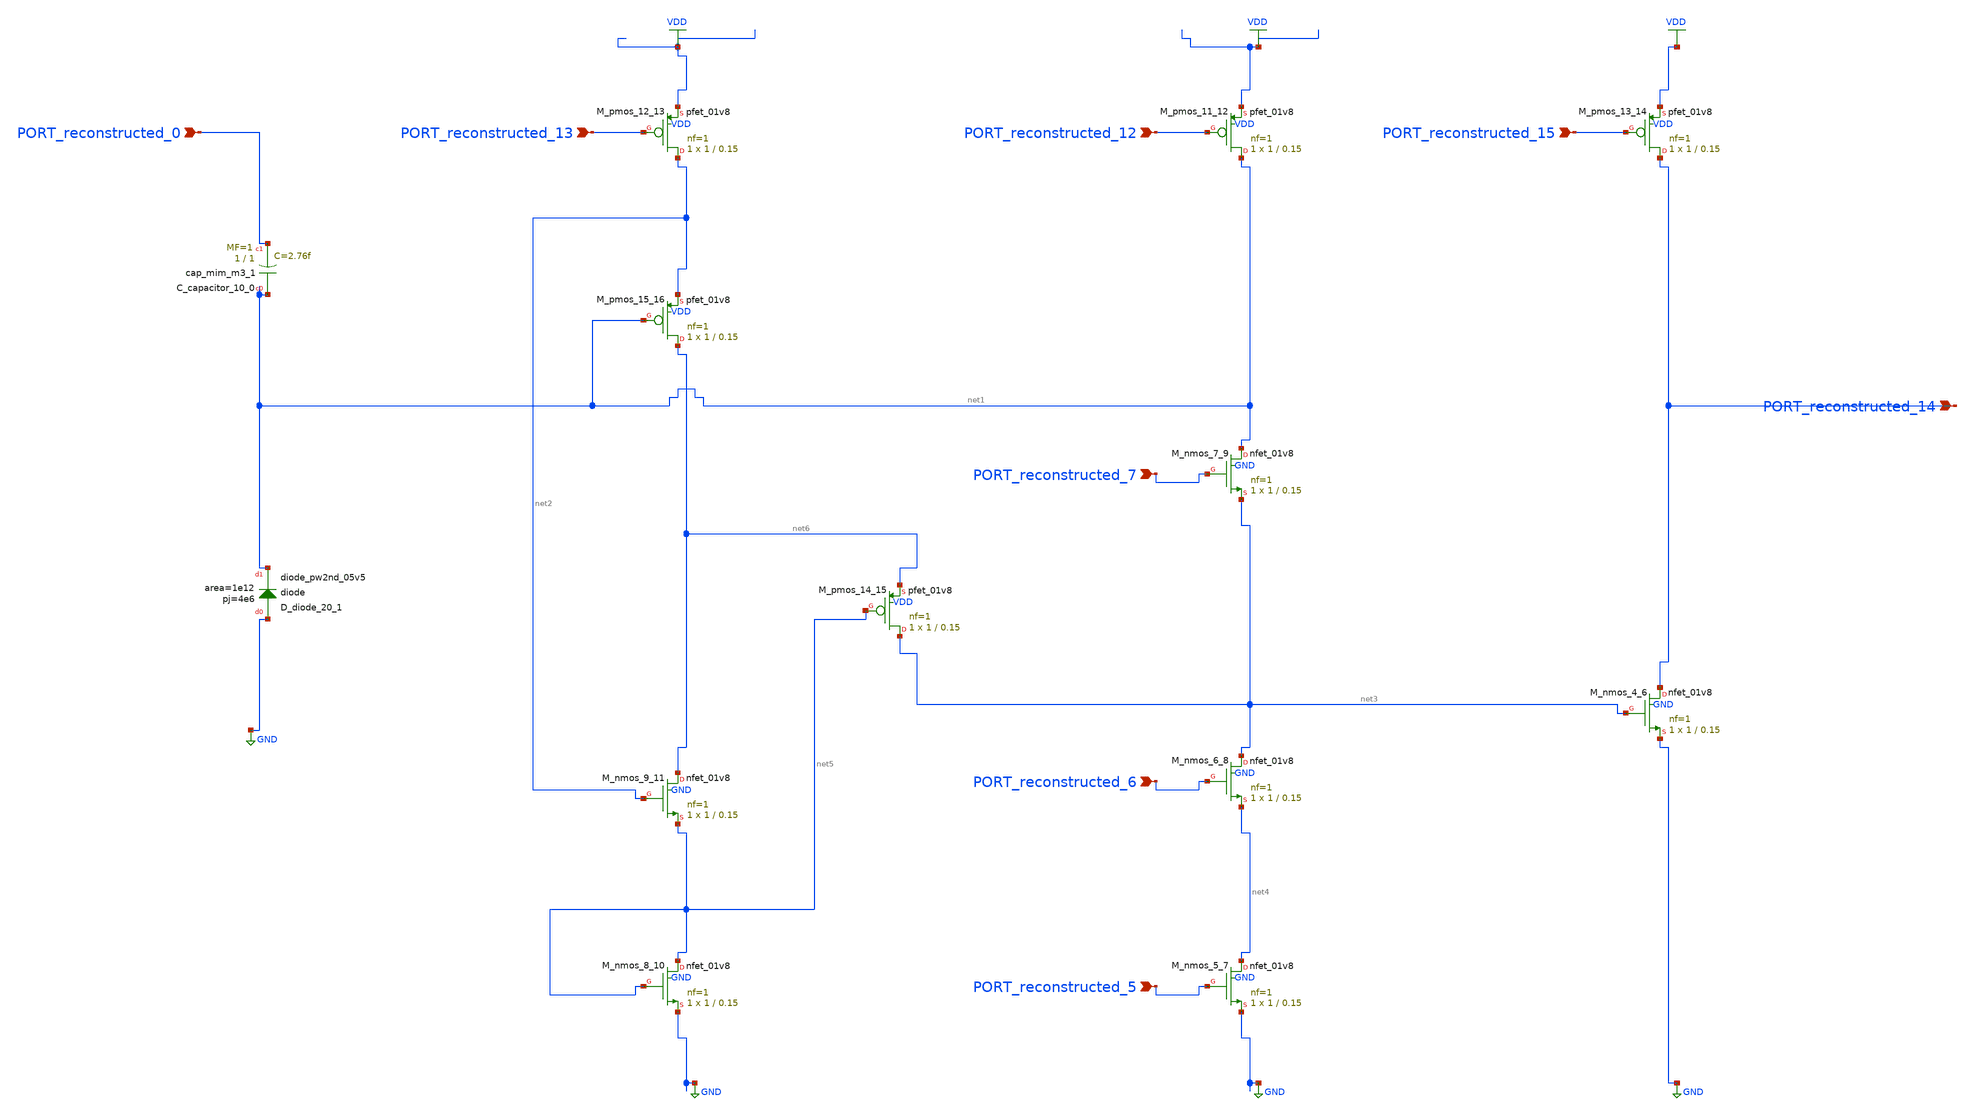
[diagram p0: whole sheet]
** sch_path: schematics/SchemGen/10_22323_1_420_0083_05_001.sch
**.subckt 10_22323_1_420_0083_05_001 PORT_reconstructed_6 PORT_reconstructed_12 PORT_reconstructed_7
*+ PORT_reconstructed_15 PORT_reconstructed_5 PORT_reconstructed_13 PORT_reconstructed_0 PORT_reconstructed_14
*.ipin PORT_reconstructed_6
*.ipin PORT_reconstructed_12
*.ipin PORT_reconstructed_7
*.ipin PORT_reconstructed_15
*.ipin PORT_reconstructed_5
*.ipin PORT_reconstructed_13
*.ipin PORT_reconstructed_0
*.ipin PORT_reconstructed_14
XC_capacitor_10_0 net1 PORT_reconstructed_0 sky130_fd_pr__cap_mim_m3_1 W=1 L=1 MF=1 m=1
XD_diode_20_1 GND net1 sky130_fd_pr__diode_pw2nd_05v5 area=1e12 pj=4e6
XM_nmos_4_6 PORT_reconstructed_14 net3 GND GND sky130_fd_pr__nfet_01v8 L=0.15 W=1 nf=1 ad='int((1 + 1)/2) * 1 / 1 * 0.29'
+ as='int((1 + 2)/2) * 1 / 1 * 0.29' pd='2*int((1 + 1)/2) * (1 / 1 + 0.29)' ps='2*int((1 + 2)/2) * (1 / 1 + 0.29)'
+ nrd='0.29 / 1 ' nrs='0.29 / 1 ' sa=0 sb=0 sd=0 mult=1 m=1
XM_nmos_5_7 net4 PORT_reconstructed_5 GND GND sky130_fd_pr__nfet_01v8 L=0.15 W=1 nf=1 ad='int((1 + 1)/2) * 1 / 1 * 0.29'
+ as='int((1 + 2)/2) * 1 / 1 * 0.29' pd='2*int((1 + 1)/2) * (1 / 1 + 0.29)' ps='2*int((1 + 2)/2) * (1 / 1 + 0.29)'
+ nrd='0.29 / 1 ' nrs='0.29 / 1 ' sa=0 sb=0 sd=0 mult=1 m=1
XM_nmos_6_8 net3 PORT_reconstructed_6 net4 GND sky130_fd_pr__nfet_01v8 L=0.15 W=1 nf=1 ad='int((1 + 1)/2) * 1 / 1 * 0.29'
+ as='int((1 + 2)/2) * 1 / 1 * 0.29' pd='2*int((1 + 1)/2) * (1 / 1 + 0.29)' ps='2*int((1 + 2)/2) * (1 / 1 + 0.29)'
+ nrd='0.29 / 1 ' nrs='0.29 / 1 ' sa=0 sb=0 sd=0 mult=1 m=1
XM_nmos_7_9 net1 PORT_reconstructed_7 net3 GND sky130_fd_pr__nfet_01v8 L=0.15 W=1 nf=1 ad='int((1 + 1)/2) * 1 / 1 * 0.29'
+ as='int((1 + 2)/2) * 1 / 1 * 0.29' pd='2*int((1 + 1)/2) * (1 / 1 + 0.29)' ps='2*int((1 + 2)/2) * (1 / 1 + 0.29)'
+ nrd='0.29 / 1 ' nrs='0.29 / 1 ' sa=0 sb=0 sd=0 mult=1 m=1
XM_nmos_8_10 net5 net5 GND GND sky130_fd_pr__nfet_01v8 L=0.15 W=1 nf=1 ad='int((1 + 1)/2) * 1 / 1 * 0.29'
+ as='int((1 + 2)/2) * 1 / 1 * 0.29' pd='2*int((1 + 1)/2) * (1 / 1 + 0.29)' ps='2*int((1 + 2)/2) * (1 / 1 + 0.29)'
+ nrd='0.29 / 1 ' nrs='0.29 / 1 ' sa=0 sb=0 sd=0 mult=1 m=1
XM_nmos_9_11 net6 net2 net5 GND sky130_fd_pr__nfet_01v8 L=0.15 W=1 nf=1 ad='int((1 + 1)/2) * 1 / 1 * 0.29'
+ as='int((1 + 2)/2) * 1 / 1 * 0.29' pd='2*int((1 + 1)/2) * (1 / 1 + 0.29)' ps='2*int((1 + 2)/2) * (1 / 1 + 0.29)'
+ nrd='0.29 / 1 ' nrs='0.29 / 1 ' sa=0 sb=0 sd=0 mult=1 m=1
XM_pmos_11_12 net1 PORT_reconstructed_12 VDD VDD sky130_fd_pr__pfet_01v8 L=0.15 W=1 nf=1 ad='int((1 + 1)/2) * 1 / 1 * 0.29'
+ as='int((1 + 2)/2) * 1 / 1 * 0.29' pd='2*int((1 + 1)/2) * (1 / 1 + 0.29)' ps='2*int((1 + 2)/2) * (1 / 1 + 0.29)'
+ nrd='0.29 / 1 ' nrs='0.29 / 1 ' sa=0 sb=0 sd=0 mult=1 m=1
XM_pmos_12_13 net2 PORT_reconstructed_13 VDD VDD sky130_fd_pr__pfet_01v8 L=0.15 W=1 nf=1 ad='int((1 + 1)/2) * 1 / 1 * 0.29'
+ as='int((1 + 2)/2) * 1 / 1 * 0.29' pd='2*int((1 + 1)/2) * (1 / 1 + 0.29)' ps='2*int((1 + 2)/2) * (1 / 1 + 0.29)'
+ nrd='0.29 / 1 ' nrs='0.29 / 1 ' sa=0 sb=0 sd=0 mult=1 m=1
XM_pmos_13_14 PORT_reconstructed_14 PORT_reconstructed_15 VDD VDD sky130_fd_pr__pfet_01v8 L=0.15 W=1
+ nf=1 ad='int((1 + 1)/2) * 1 / 1 * 0.29' as='int((1 + 2)/2) * 1 / 1 * 0.29' pd='2*int((1 + 1)/2) * (1 / 1 + 0.29)'
+ ps='2*int((1 + 2)/2) * (1 / 1 + 0.29)' nrd='0.29 / 1 ' nrs='0.29 / 1 ' sa=0 sb=0 sd=0 mult=1 m=1
XM_pmos_14_15 net3 net5 net6 VDD sky130_fd_pr__pfet_01v8 L=0.15 W=1 nf=1 ad='int((1 + 1)/2) * 1 / 1 * 0.29'
+ as='int((1 + 2)/2) * 1 / 1 * 0.29' pd='2*int((1 + 1)/2) * (1 / 1 + 0.29)' ps='2*int((1 + 2)/2) * (1 / 1 + 0.29)'
+ nrd='0.29 / 1 ' nrs='0.29 / 1 ' sa=0 sb=0 sd=0 mult=1 m=1
XM_pmos_15_16 net6 net1 net2 VDD sky130_fd_pr__pfet_01v8 L=0.15 W=1 nf=1 ad='int((1 + 1)/2) * 1 / 1 * 0.29'
+ as='int((1 + 2)/2) * 1 / 1 * 0.29' pd='2*int((1 + 1)/2) * (1 / 1 + 0.29)' ps='2*int((1 + 2)/2) * (1 / 1 + 0.29)'
+ nrd='0.29 / 1 ' nrs='0.29 / 1 ' sa=0 sb=0 sd=0 mult=1 m=1
**.ends
.GLOBAL GND
.GLOBAL VDD
.end
